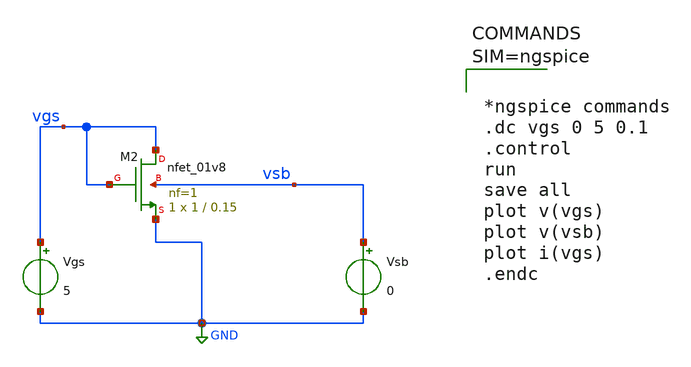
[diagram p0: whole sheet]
** sch_path: xschem/nmos1.sch
**.subckt nmos1
Vgs vgs GND 5
Vsb vsb GND 0
XM2 vgs vgs GND vsb sky130_fd_pr__nfet_01v8 L=0.15 W=1 nf=1 ad='int((1 + 1)/2) * 1 / 1 * 0.29' as='int((1 + 2)/2) * 1 / 1 * 0.29'
+ pd='2*int((1 + 1)/2) * (1 / 1 + 0.29)' ps='2*int((1 + 2)/2) * (1 / 1 + 0.29)' nrd='0.29 / 1 ' nrs='0.29 / 1 '
+ sa=0 sb=0 sd=0 mult=1 m=1
**** begin user architecture code

** opencircuitdesign pdks install
.lib $::SKYWATER_MODELS/sky130.lib.spice tt




*ngspice commands
.dc vgs 0 5 0.1
.control
run
save all
plot v(vgs)
plot v(vsb)
plot i(vgs)
.endc



**** end user architecture code
**.ends
.GLOBAL GND
.end
